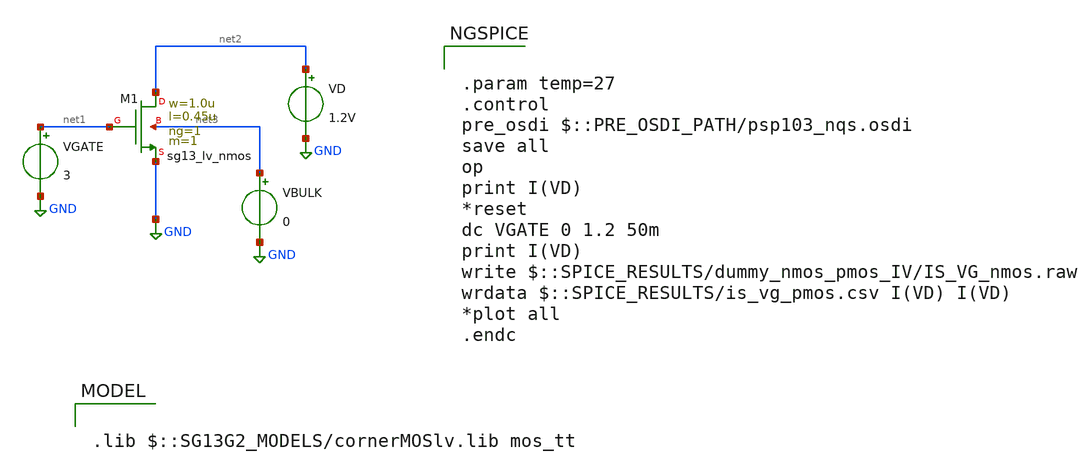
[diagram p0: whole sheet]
** sch_path: exp/IHP130/dummy_nmos_IV/pmos_IS_vs_VG.sch
**.subckt pmos_IS_vs_VG
XM1 net2 net1 GND net3 sg13_lv_nmos w=1.0u l=0.45u ng=1 m=1 mm_ok=1
VGATE net1 GND 3
VD net2 GND 1.2V
VBULK net3 GND 0
**** begin user architecture code

.param temp=27
.control
pre_osdi $::PRE_OSDI_PATH/psp103_nqs.osdi
save all
op
print I(VD)
*reset
dc VGATE 0 1.2 50m
print I(VD)
write $::SPICE_RESULTS/dummy_nmos_pmos_IV/IS_VG_nmos.raw
wrdata $::SPICE_RESULTS/is_vg_pmos.csv I(VD) I(VD)
*plot all
.endc


.lib $::SG13G2_MODELS/cornerMOSlv.lib mos_tt

**** end user architecture code
**.ends
.GLOBAL GND
.end
